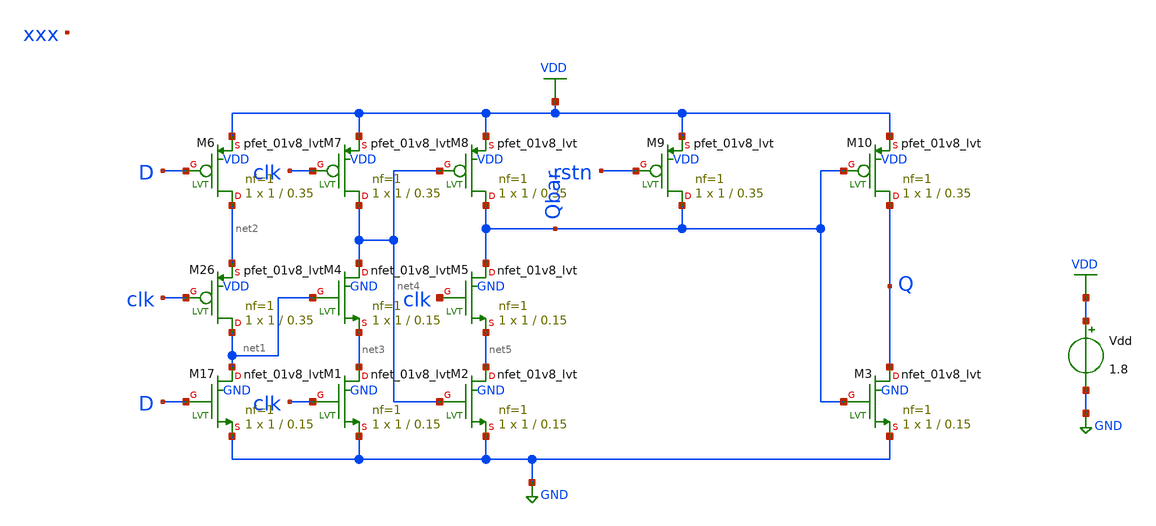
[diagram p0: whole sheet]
** sch_path: pll/pfd_cp_lf_lib/DFF/xschem/DFF.sch
**.subckt DFF
XM17 net1 D GND GND sky130_fd_pr__nfet_01v8_lvt L=0.15 W=1 nf=1 ad='int((1 + 1)/2) * 1 / 1 * 0.29' as='int((1 + 2)/2) * 1 / 1 * 0.29'
+ pd='2*int((1 + 1)/2) * (1 / 1 + 0.29)' ps='2*int((1 + 2)/2) * (1 / 1 + 0.29)' nrd='0.29 / 1 ' nrs='0.29 / 1 '
+ sa=0 sb=0 sd=0 mult=1 m=1
XM1 net3 clk GND GND sky130_fd_pr__nfet_01v8_lvt L=0.15 W=1 nf=1 ad='int((1 + 1)/2) * 1 / 1 * 0.29' as='int((1 + 2)/2) * 1 / 1 * 0.29'
+ pd='2*int((1 + 1)/2) * (1 / 1 + 0.29)' ps='2*int((1 + 2)/2) * (1 / 1 + 0.29)' nrd='0.29 / 1 ' nrs='0.29 / 1 '
+ sa=0 sb=0 sd=0 mult=1 m=1
XM2 net5 net4 GND GND sky130_fd_pr__nfet_01v8_lvt L=0.15 W=1 nf=1 ad='int((1 + 1)/2) * 1 / 1 * 0.29'
+ as='int((1 + 2)/2) * 1 / 1 * 0.29' pd='2*int((1 + 1)/2) * (1 / 1 + 0.29)' ps='2*int((1 + 2)/2) * (1 / 1 + 0.29)'
+ nrd='0.29 / 1 ' nrs='0.29 / 1 ' sa=0 sb=0 sd=0 mult=1 m=1
XM3 Q Qbar GND GND sky130_fd_pr__nfet_01v8_lvt L=0.15 W=1 nf=1 ad='int((1 + 1)/2) * 1 / 1 * 0.29' as='int((1 + 2)/2) * 1 / 1 * 0.29'
+ pd='2*int((1 + 1)/2) * (1 / 1 + 0.29)' ps='2*int((1 + 2)/2) * (1 / 1 + 0.29)' nrd='0.29 / 1 ' nrs='0.29 / 1 '
+ sa=0 sb=0 sd=0 mult=1 m=1
XM4 net4 net1 net3 GND sky130_fd_pr__nfet_01v8_lvt L=0.15 W=1 nf=1 ad='int((1 + 1)/2) * 1 / 1 * 0.29'
+ as='int((1 + 2)/2) * 1 / 1 * 0.29' pd='2*int((1 + 1)/2) * (1 / 1 + 0.29)' ps='2*int((1 + 2)/2) * (1 / 1 + 0.29)'
+ nrd='0.29 / 1 ' nrs='0.29 / 1 ' sa=0 sb=0 sd=0 mult=1 m=1
XM5 Qbar clk net5 GND sky130_fd_pr__nfet_01v8_lvt L=0.15 W=1 nf=1 ad='int((1 + 1)/2) * 1 / 1 * 0.29'
+ as='int((1 + 2)/2) * 1 / 1 * 0.29' pd='2*int((1 + 1)/2) * (1 / 1 + 0.29)' ps='2*int((1 + 2)/2) * (1 / 1 + 0.29)'
+ nrd='0.29 / 1 ' nrs='0.29 / 1 ' sa=0 sb=0 sd=0 mult=1 m=1
XM26 net1 clk net2 VDD sky130_fd_pr__pfet_01v8_lvt L=0.35 W=1 nf=1 ad='int((1 + 1)/2) * 1 / 1 * 0.29'
+ as='int((1 + 2)/2) * 1 / 1 * 0.29' pd='2*int((1 + 1)/2) * (1 / 1 + 0.29)' ps='2*int((1 + 2)/2) * (1 / 1 + 0.29)'
+ nrd='0.29 / 1 ' nrs='0.29 / 1 ' sa=0 sb=0 sd=0 mult=1 m=1
XM6 net2 D VDD VDD sky130_fd_pr__pfet_01v8_lvt L=0.35 W=1 nf=1 ad='int((1 + 1)/2) * 1 / 1 * 0.29' as='int((1 + 2)/2) * 1 / 1 * 0.29'
+ pd='2*int((1 + 1)/2) * (1 / 1 + 0.29)' ps='2*int((1 + 2)/2) * (1 / 1 + 0.29)' nrd='0.29 / 1 ' nrs='0.29 / 1 '
+ sa=0 sb=0 sd=0 mult=1 m=1
XM7 net4 clk VDD VDD sky130_fd_pr__pfet_01v8_lvt L=0.35 W=1 nf=1 ad='int((1 + 1)/2) * 1 / 1 * 0.29' as='int((1 + 2)/2) * 1 / 1 * 0.29'
+ pd='2*int((1 + 1)/2) * (1 / 1 + 0.29)' ps='2*int((1 + 2)/2) * (1 / 1 + 0.29)' nrd='0.29 / 1 ' nrs='0.29 / 1 '
+ sa=0 sb=0 sd=0 mult=1 m=1
XM8 Qbar net4 VDD VDD sky130_fd_pr__pfet_01v8_lvt L=0.35 W=1 nf=1 ad='int((1 + 1)/2) * 1 / 1 * 0.29'
+ as='int((1 + 2)/2) * 1 / 1 * 0.29' pd='2*int((1 + 1)/2) * (1 / 1 + 0.29)' ps='2*int((1 + 2)/2) * (1 / 1 + 0.29)'
+ nrd='0.29 / 1 ' nrs='0.29 / 1 ' sa=0 sb=0 sd=0 mult=1 m=1
XM9 Qbar rstn VDD VDD sky130_fd_pr__pfet_01v8_lvt L=0.35 W=1 nf=1 ad='int((1 + 1)/2) * 1 / 1 * 0.29'
+ as='int((1 + 2)/2) * 1 / 1 * 0.29' pd='2*int((1 + 1)/2) * (1 / 1 + 0.29)' ps='2*int((1 + 2)/2) * (1 / 1 + 0.29)'
+ nrd='0.29 / 1 ' nrs='0.29 / 1 ' sa=0 sb=0 sd=0 mult=1 m=1
XM10 Q Qbar VDD VDD sky130_fd_pr__pfet_01v8_lvt L=0.35 W=1 nf=1 ad='int((1 + 1)/2) * 1 / 1 * 0.29' as='int((1 + 2)/2) * 1 / 1 * 0.29'
+ pd='2*int((1 + 1)/2) * (1 / 1 + 0.29)' ps='2*int((1 + 2)/2) * (1 / 1 + 0.29)' nrd='0.29 / 1 ' nrs='0.29 / 1 '
+ sa=0 sb=0 sd=0 mult=1 m=1
Vdd VDD GND 1.8
**.ends
.GLOBAL GND
.GLOBAL VDD
.end
